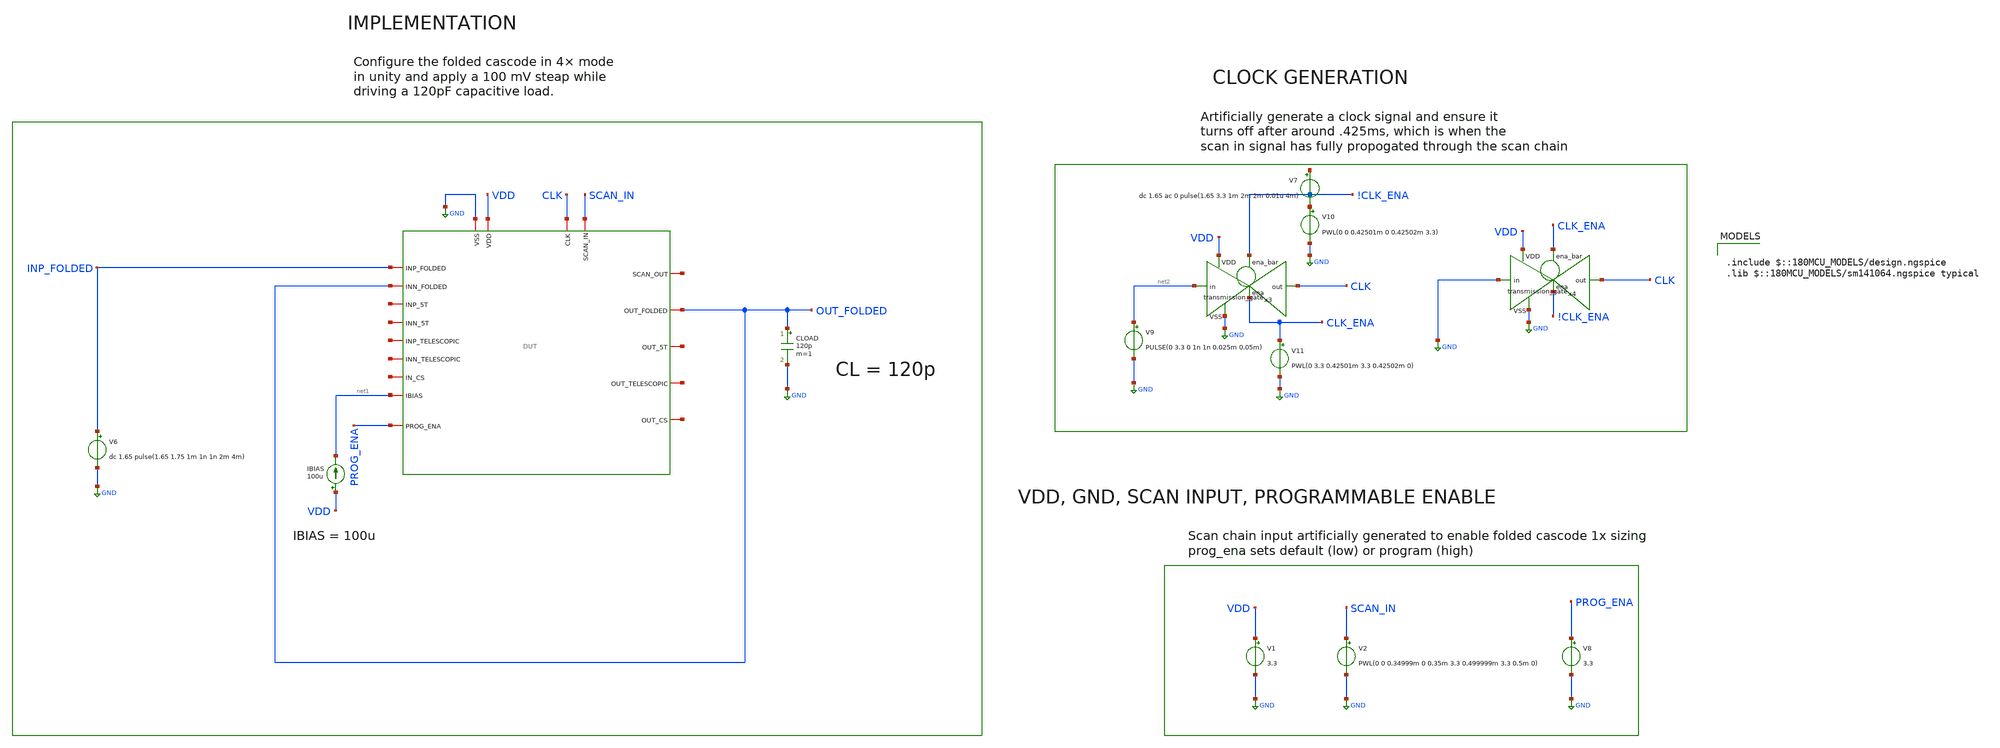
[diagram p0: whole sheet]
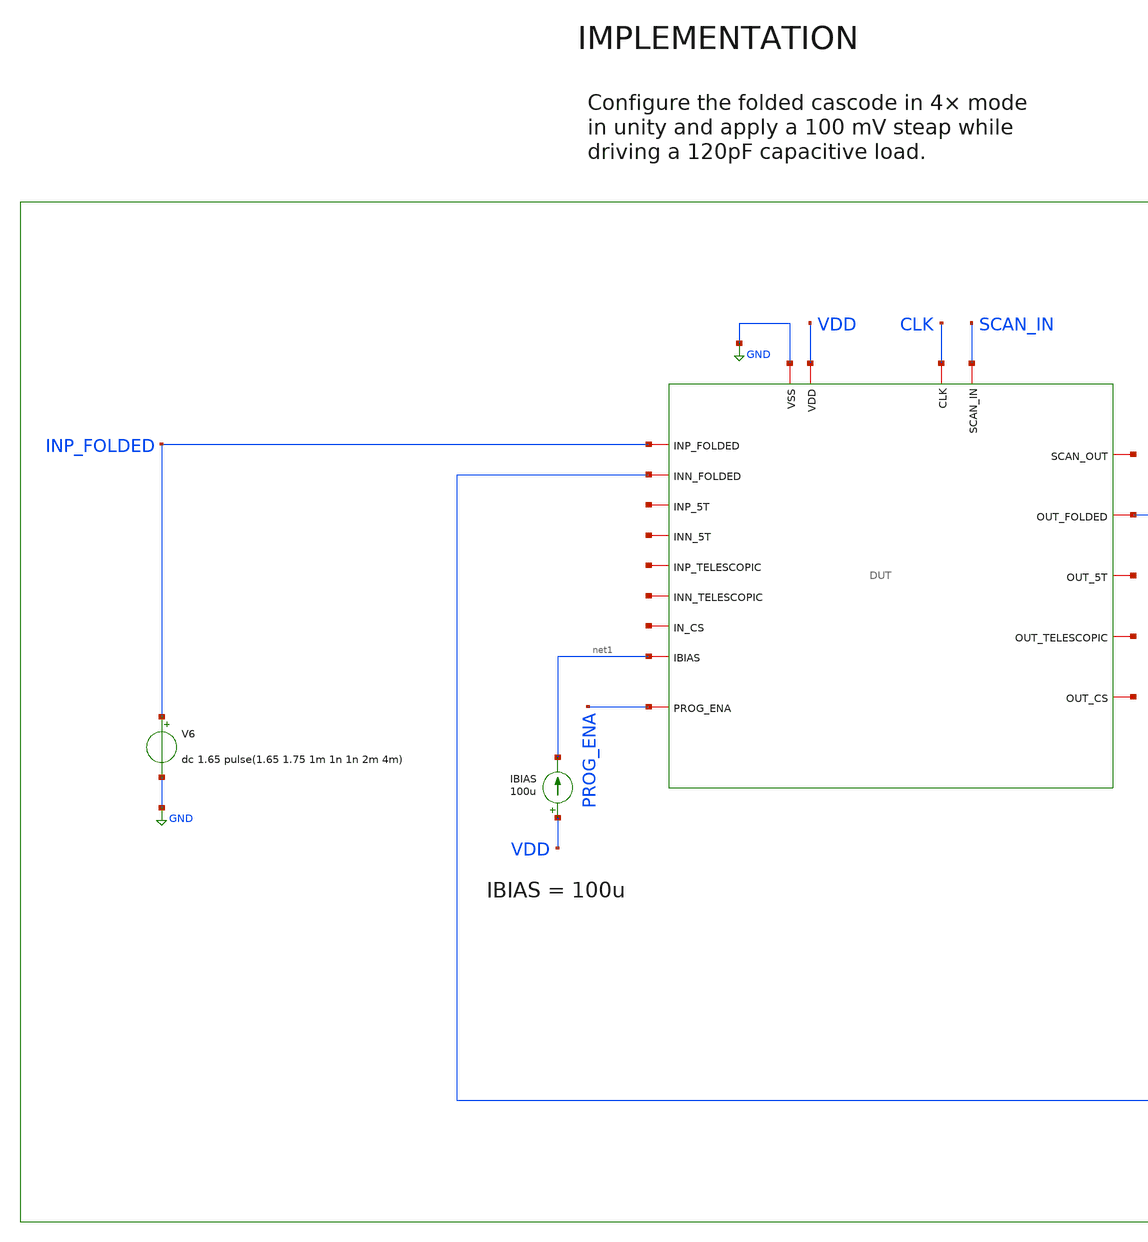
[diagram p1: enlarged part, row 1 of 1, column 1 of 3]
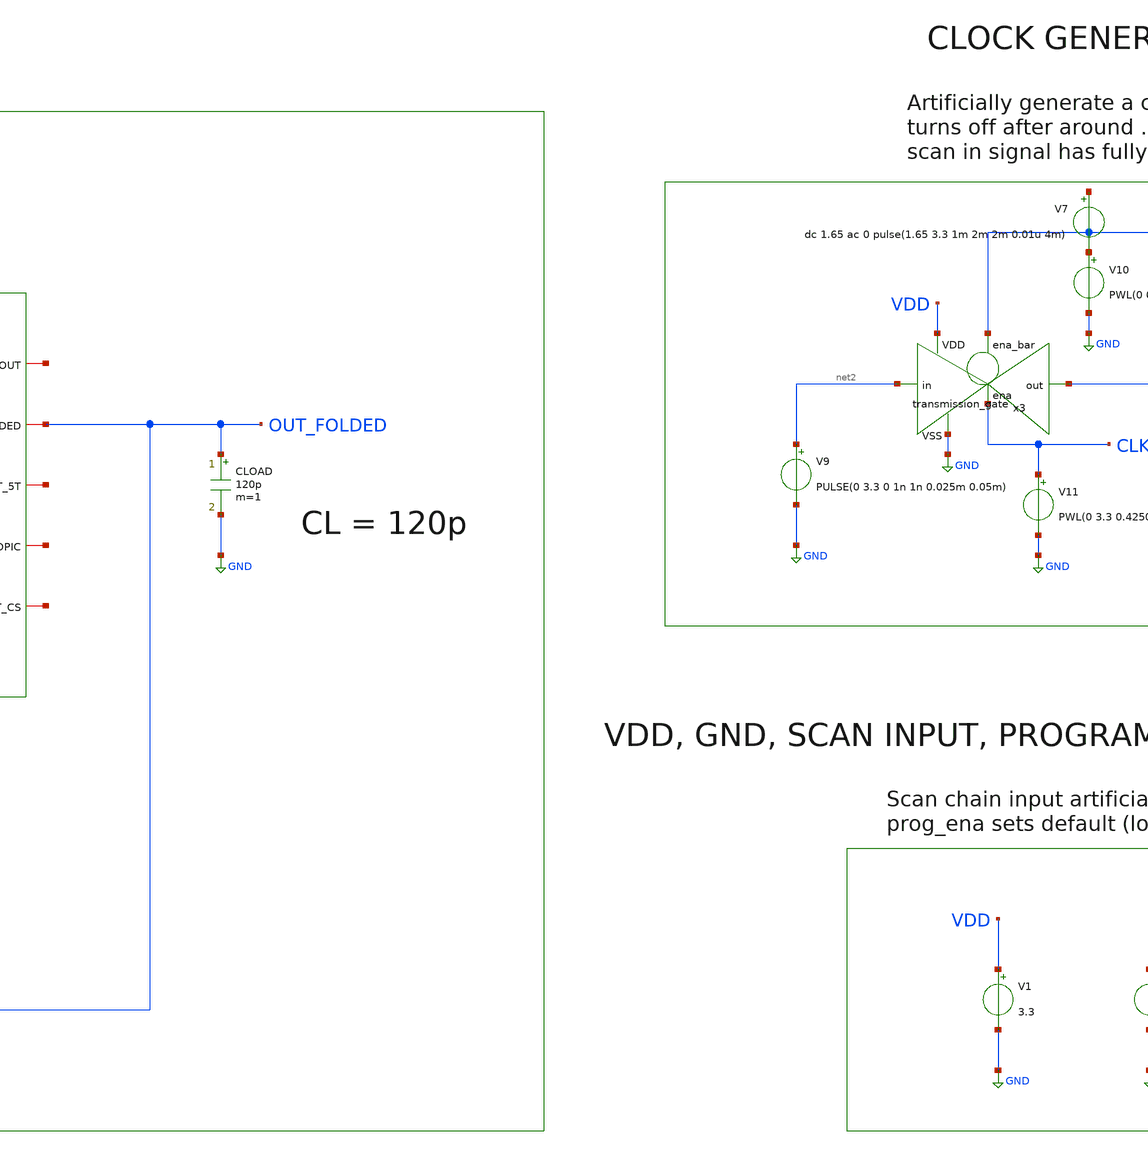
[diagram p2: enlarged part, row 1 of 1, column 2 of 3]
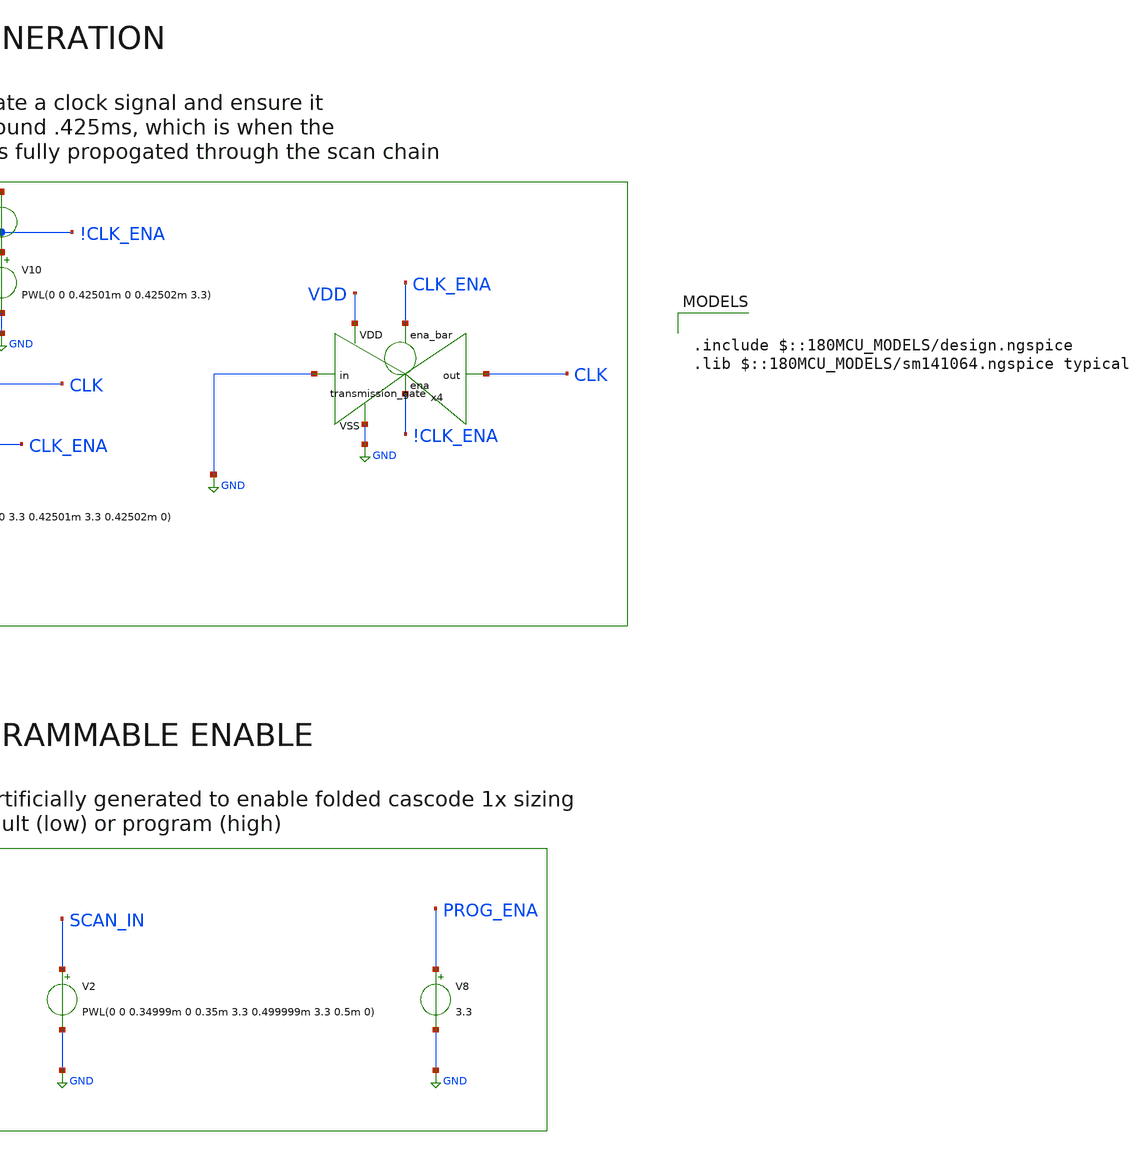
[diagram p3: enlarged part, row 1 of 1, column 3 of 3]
** sch_path: designs/libs/verification/ota_folded/4x_sizing/step_response_tb.sch
**.subckt step_response_tb
V1 VDD GND 3.3
IBIAS VDD net1 100u
CLOAD OUT_FOLDED GND 120p m=1
x1 CLK net3 SCAN_IN GND VDD OUT_FOLDED INP_FOLDED net4 net1 OUT_FOLDED net5 net6 net7 net8 net9
+ net10 net11 PROG_ENA DUT
V8 PROG_ENA GND 3.3
V9 net2 GND PULSE(0 3.3 0 1n 1n 0.025m 0.05m)
x3 !CLK_ENA VDD CLK net2 GND CLK_ENA transmission_gate
V10 !CLK_ENA GND PWL(0 0 0.42501m 0 0.42502m 3.3)
V11 CLK_ENA GND PWL(0 3.3 0.42501m 3.3 0.42502m 0)
x4 CLK_ENA VDD CLK GND GND !CLK_ENA transmission_gate
V6 INP_FOLDED GND dc 1.65 pulse(1.65 1.75 1m 1n 1n 2m 4m)
V2 SCAN_IN GND PWL(0 0 0.34999m 0 0.35m 3.3 0.499999m 3.3 0.5m 0)
V7 net12 !CLK_ENA dc 1.65 ac 0 pulse(1.65 3.3 1m 2m 2m 0.01u 4m)
**** begin user architecture code

.include $::180MCU_MODELS/design.ngspice
.lib $::180MCU_MODELS/sm141064.ngspice typical



.control
tran 1u 5m

plot v(out_folded) v(inp_folded)

meas tran v_before find v(out_folded) at=0.99m
meas tran v_after find v(out_folded) at=2.5m

let delta = v_after - v_before
let t20_val = v_before + 0.2 * delta
let t80_val = v_before + 0.8 * delta

meas tran t_20 when v(out_folded) = t20_val rise = 1
meas tran t_80 when v(out_folded) = t80_val rise = 1
let sr_rise = delta / (t_80 - t_20)
print sr_rise

meas tran t_20f when v(out_folded) = t80_val fall = 1
meas tran t_80f when v(out_folded) = t20_val fall = 1
let sr_fall = delta / (t_80f - t_20f)
print sr_fall

meas tran vpeak max v(out_folded) from=1m to=3m
let overshoot = (vpeak - v_after) / delta * 100
print overshoot

meas tran t_settle when v(out_folded) = v_after td = 1m rise = 1
let settling = t_settle - 1m
print settling

print v_before v_after delta
.endc


**** end user architecture code
**.ends
.GLOBAL GND
.end
